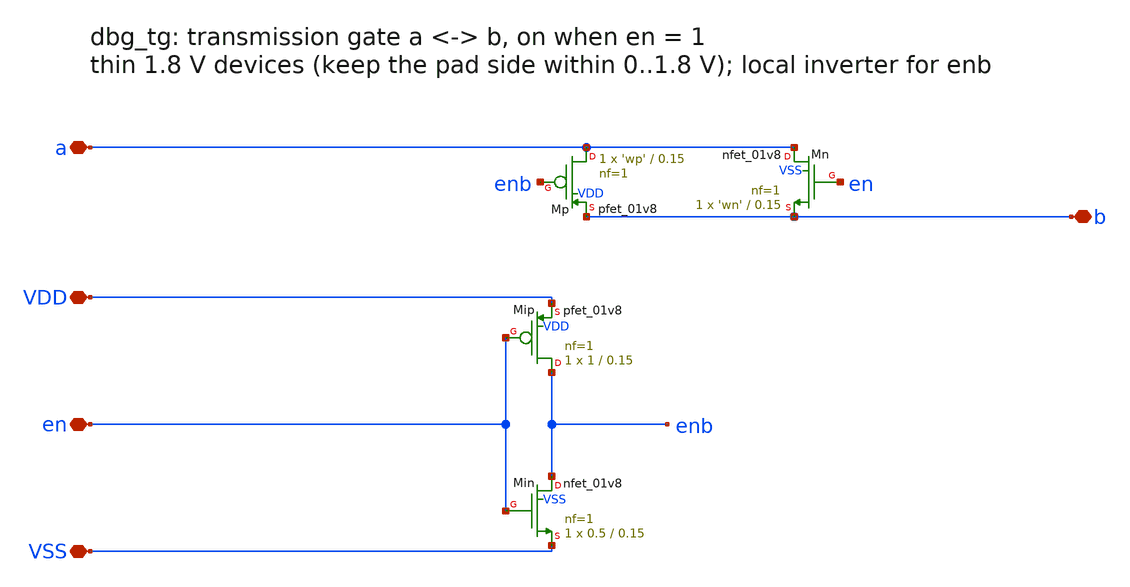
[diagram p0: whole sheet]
** sch_path: xschem/dbg_tg.sch
**.subckt dbg_tg VDD VSS en a b
*.iopin VDD
*.iopin VSS
*.iopin en
*.iopin a
*.iopin b
XMip enb en VDD VDD sky130_fd_pr__pfet_01v8 L=0.15 W=1 nf=1 ad='int((nf+1)/2) * W/nf * 0.29' as='int((nf+2)/2) * W/nf * 0.29'
+ pd='2*int((nf+1)/2) * (W/nf + 0.29)' ps='2*int((nf+2)/2) * (W/nf + 0.29)' nrd='0.29 / W' nrs='0.29 / W'
+ sa=0 sb=0 sd=0 mult=1 m=1
XMin enb en VSS VSS sky130_fd_pr__nfet_01v8 L=0.15 W=0.5 nf=1 ad='int((nf+1)/2) * W/nf * 0.29' as='int((nf+2)/2) * W/nf * 0.29'
+ pd='2*int((nf+1)/2) * (W/nf + 0.29)' ps='2*int((nf+2)/2) * (W/nf + 0.29)' nrd='0.29 / W' nrs='0.29 / W'
+ sa=0 sb=0 sd=0 mult=1 m=1
XMn a en b VSS sky130_fd_pr__nfet_01v8 L=0.15 W='wn' nf=1 ad='int((nf+1)/2) * W/nf * 0.29' as='int((nf+2)/2) * W/nf * 0.29'
+ pd='2*int((nf+1)/2) * (W/nf + 0.29)' ps='2*int((nf+2)/2) * (W/nf + 0.29)' nrd='0.29 / W' nrs='0.29 / W'
+ sa=0 sb=0 sd=0 mult=1 m=1
XMp a enb b VDD sky130_fd_pr__pfet_01v8 L=0.15 W='wp' nf=1 ad='int((nf+1)/2) * W/nf * 0.29' as='int((nf+2)/2) * W/nf * 0.29'
+ pd='2*int((nf+1)/2) * (W/nf + 0.29)' ps='2*int((nf+2)/2) * (W/nf + 0.29)' nrd='0.29 / W' nrs='0.29 / W'
+ sa=0 sb=0 sd=0 mult=1 m=1
**.ends
.end
